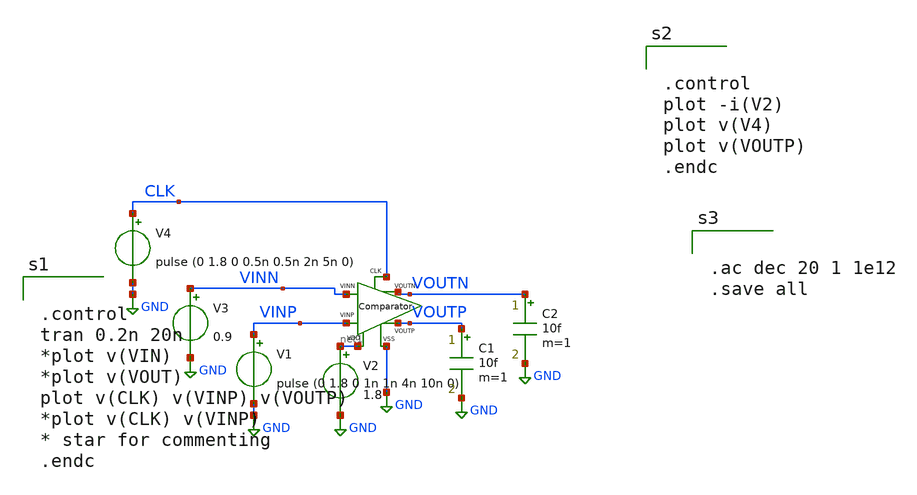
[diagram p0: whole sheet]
** sch_path: xschem/xschem_BGR_Top/Sigma_Delta/Comparator/Comparator_TB.sch
**.subckt Comparator_TB
XCOMP1 VINN VINP net2 VOUTP CLK net1 GND Comparator
V1 VINP GND pulse (0 1.8 0 1n 1n 4n 10n 0)
V2 net1 GND 1.8
V3 VINN GND 0.9
V4 CLK GND pulse (0 1.8 0 0.5n 0.5n 2n 5n 0)
C1 VOUTP GND 10f m=1
C2 VOUTN GND 10f m=1
**** begin user architecture code


.control
tran 0.2n 20n
*plot v(VIN)
*plot v(VOUT)
plot v(CLK) v(VINP) v(VOUTP)
*plot v(CLK) v(VINP)
* star for commenting
.endc


** opencircuitdesign pdks install
.lib $::SKYWATER_MODELS/sky130.lib.spice tt




.ac dec 20 1 1e12
.save all



.control
plot -i(V2)
plot v(V4)
plot v(VOUTP)
.endc


**** end user architecture code
**.ends

* expanding   symbol:  Sigma_Delta/Comparator/Comparator.sym # of pins=7
** sym_path: xschem/xschem_BGR_Top/Sigma_Delta/Comparator/Comparator.sym
** sch_path: xschem/xschem_BGR_Top/Sigma_Delta/Comparator/Comparator.sch
.subckt Comparator VINN VINP VOUTN VOUTP CLK VDD VSS
*.iopin VDD
*.iopin VSS
*.iopin VOUTP
*.iopin VOUTN
*.iopin VINP
*.iopin VINN
*.iopin CLK
XM16 net1 net4 net2 VSS sky130_fd_pr__nfet_01v8 L=0.15 W=0.5 nf=1 ad='int((nf+1)/2) * W/nf * 0.29' as='int((nf+2)/2) * W/nf * 0.29'
+ pd='2*int((nf+1)/2) * (W/nf + 0.29)' ps='2*int((nf+2)/2) * (W/nf + 0.29)' nrd='0.29 / W' nrs='0.29 / W'
+ sa=0 sb=0 sd=0 mult=1 m=1
XM17 net1 net4 VDD VDD sky130_fd_pr__pfet_01v8 L=0.15 W=1 nf=1 ad='int((nf+1)/2) * W/nf * 0.29' as='int((nf+2)/2) * W/nf * 0.29'
+ pd='2*int((nf+1)/2) * (W/nf + 0.29)' ps='2*int((nf+2)/2) * (W/nf + 0.29)' nrd='0.29 / W' nrs='0.29 / W'
+ sa=0 sb=0 sd=0 mult=1 m=1
XM18 net2 VINN net3 VSS sky130_fd_pr__nfet_01v8 L=0.15 W=2 nf=1 ad='int((nf+1)/2) * W/nf * 0.29' as='int((nf+2)/2) * W/nf * 0.29'
+ pd='2*int((nf+1)/2) * (W/nf + 0.29)' ps='2*int((nf+2)/2) * (W/nf + 0.29)' nrd='0.29 / W' nrs='0.29 / W'
+ sa=0 sb=0 sd=0 mult=1 m=1
XM19 net1 CLK VDD VDD sky130_fd_pr__pfet_01v8 L=0.15 W=1 nf=1 ad='int((nf+1)/2) * W/nf * 0.29' as='int((nf+2)/2) * W/nf * 0.29'
+ pd='2*int((nf+1)/2) * (W/nf + 0.29)' ps='2*int((nf+2)/2) * (W/nf + 0.29)' nrd='0.29 / W' nrs='0.29 / W'
+ sa=0 sb=0 sd=0 mult=1 m=1
XM20 net2 CLK VDD VDD sky130_fd_pr__pfet_01v8 L=0.15 W=1 nf=1 ad='int((nf+1)/2) * W/nf * 0.29' as='int((nf+2)/2) * W/nf * 0.29'
+ pd='2*int((nf+1)/2) * (W/nf + 0.29)' ps='2*int((nf+2)/2) * (W/nf + 0.29)' nrd='0.29 / W' nrs='0.29 / W'
+ sa=0 sb=0 sd=0 mult=1 m=1
XM21 VOUTN net1 VSS VSS sky130_fd_pr__nfet_01v8 L=0.15 W=2 nf=1 ad='int((nf+1)/2) * W/nf * 0.29' as='int((nf+2)/2) * W/nf * 0.29'
+ pd='2*int((nf+1)/2) * (W/nf + 0.29)' ps='2*int((nf+2)/2) * (W/nf + 0.29)' nrd='0.29 / W' nrs='0.29 / W'
+ sa=0 sb=0 sd=0 mult=1 m=1
XM22 VOUTN net1 VDD VDD sky130_fd_pr__pfet_01v8 L=0.15 W=4 nf=1 ad='int((nf+1)/2) * W/nf * 0.29' as='int((nf+2)/2) * W/nf * 0.29'
+ pd='2*int((nf+1)/2) * (W/nf + 0.29)' ps='2*int((nf+2)/2) * (W/nf + 0.29)' nrd='0.29 / W' nrs='0.29 / W'
+ sa=0 sb=0 sd=0 mult=1 m=1
XM23 net4 net1 net5 VSS sky130_fd_pr__nfet_01v8 L=0.15 W=0.5 nf=1 ad='int((nf+1)/2) * W/nf * 0.29' as='int((nf+2)/2) * W/nf * 0.29'
+ pd='2*int((nf+1)/2) * (W/nf + 0.29)' ps='2*int((nf+2)/2) * (W/nf + 0.29)' nrd='0.29 / W' nrs='0.29 / W'
+ sa=0 sb=0 sd=0 mult=1 m=1
XM24 net4 net1 VDD VDD sky130_fd_pr__pfet_01v8 L=0.15 W=1 nf=1 ad='int((nf+1)/2) * W/nf * 0.29' as='int((nf+2)/2) * W/nf * 0.29'
+ pd='2*int((nf+1)/2) * (W/nf + 0.29)' ps='2*int((nf+2)/2) * (W/nf + 0.29)' nrd='0.29 / W' nrs='0.29 / W'
+ sa=0 sb=0 sd=0 mult=1 m=1
XM25 net5 VINP net3 VSS sky130_fd_pr__nfet_01v8 L=0.15 W=2 nf=1 ad='int((nf+1)/2) * W/nf * 0.29' as='int((nf+2)/2) * W/nf * 0.29'
+ pd='2*int((nf+1)/2) * (W/nf + 0.29)' ps='2*int((nf+2)/2) * (W/nf + 0.29)' nrd='0.29 / W' nrs='0.29 / W'
+ sa=0 sb=0 sd=0 mult=1 m=1
XM26 net4 CLK VDD VDD sky130_fd_pr__pfet_01v8 L=0.15 W=1 nf=1 ad='int((nf+1)/2) * W/nf * 0.29' as='int((nf+2)/2) * W/nf * 0.29'
+ pd='2*int((nf+1)/2) * (W/nf + 0.29)' ps='2*int((nf+2)/2) * (W/nf + 0.29)' nrd='0.29 / W' nrs='0.29 / W'
+ sa=0 sb=0 sd=0 mult=1 m=1
XM27 net5 CLK VDD VDD sky130_fd_pr__pfet_01v8 L=0.15 W=1 nf=1 ad='int((nf+1)/2) * W/nf * 0.29' as='int((nf+2)/2) * W/nf * 0.29'
+ pd='2*int((nf+1)/2) * (W/nf + 0.29)' ps='2*int((nf+2)/2) * (W/nf + 0.29)' nrd='0.29 / W' nrs='0.29 / W'
+ sa=0 sb=0 sd=0 mult=1 m=1
XM28 VOUTP net4 VSS VSS sky130_fd_pr__nfet_01v8 L=0.15 W=2 nf=1 ad='int((nf+1)/2) * W/nf * 0.29' as='int((nf+2)/2) * W/nf * 0.29'
+ pd='2*int((nf+1)/2) * (W/nf + 0.29)' ps='2*int((nf+2)/2) * (W/nf + 0.29)' nrd='0.29 / W' nrs='0.29 / W'
+ sa=0 sb=0 sd=0 mult=1 m=1
XM29 VOUTP net4 VDD VDD sky130_fd_pr__pfet_01v8 L=0.15 W=4 nf=1 ad='int((nf+1)/2) * W/nf * 0.29' as='int((nf+2)/2) * W/nf * 0.29'
+ pd='2*int((nf+1)/2) * (W/nf + 0.29)' ps='2*int((nf+2)/2) * (W/nf + 0.29)' nrd='0.29 / W' nrs='0.29 / W'
+ sa=0 sb=0 sd=0 mult=1 m=1
XM30 net3 CLK VSS VSS sky130_fd_pr__nfet_01v8 L=0.15 W=0.5 nf=1 ad='int((nf+1)/2) * W/nf * 0.29' as='int((nf+2)/2) * W/nf * 0.29'
+ pd='2*int((nf+1)/2) * (W/nf + 0.29)' ps='2*int((nf+2)/2) * (W/nf + 0.29)' nrd='0.29 / W' nrs='0.29 / W'
+ sa=0 sb=0 sd=0 mult=1 m=1
.ends

.GLOBAL GND
.end
